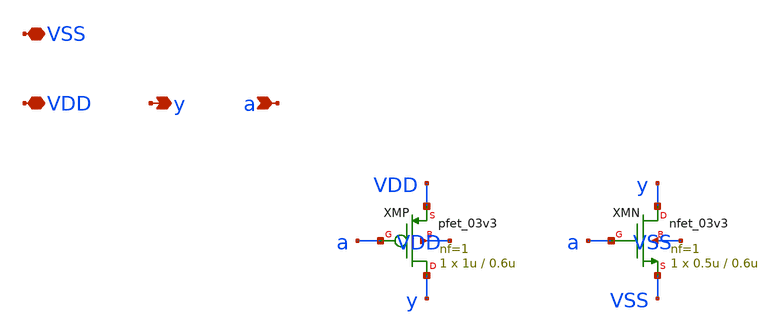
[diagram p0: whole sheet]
** sch_path: design/inv_dly.sch
**.subckt inv_dly a y VDD VSS
*.ipin a
*.opin y
*.iopin VDD
*.iopin VSS
XMP y a VDD VDD pfet_03v3 L=0.6u W=1u nf=1 ad='int((nf+1)/2) * W/nf * 0.18u' as='int((nf+2)/2) * W/nf * 0.18u'
+ pd='2*int((nf+1)/2) * (W/nf + 0.18u)' ps='2*int((nf+2)/2) * (W/nf + 0.18u)' nrd='0.18u / W' nrs='0.18u / W'
+ sa=0 sb=0 sd=0 m=1
XMN y a VSS VSS nfet_03v3 L=0.6u W=0.5u nf=1 ad='int((nf+1)/2) * W/nf * 0.18u' as='int((nf+2)/2) * W/nf * 0.18u'
+ pd='2*int((nf+1)/2) * (W/nf + 0.18u)' ps='2*int((nf+2)/2) * (W/nf + 0.18u)' nrd='0.18u / W' nrs='0.18u / W'
+ sa=0 sb=0 sd=0 m=1
**.ends
.end
